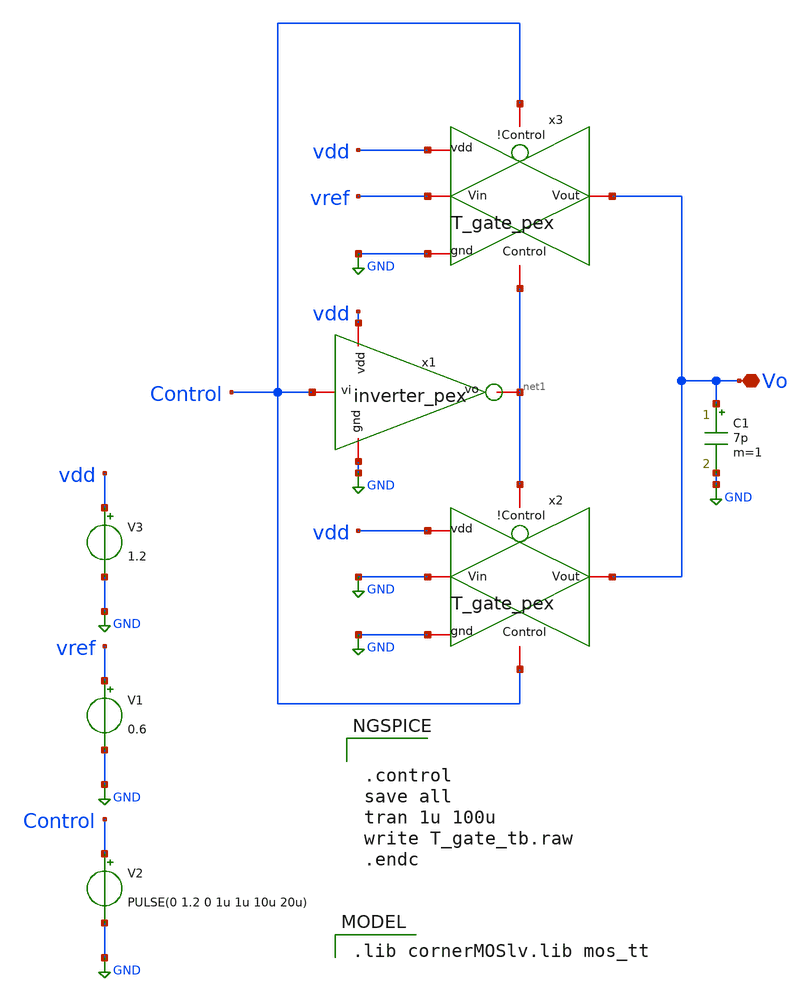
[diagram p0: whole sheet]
** sch_path: dependencies/ADC/ADC-main/schematic/xschem/T_gate_switch_tb_ps.sch
**.subckt T_gate_switch_tb_ps Vo
*.iopin Vo
V1 vref GND 0.6
V2 Control GND PULSE(0 1.2 0 1u 1u 10u 20u)
V3 vdd GND 1.2
C1 Vo GND 7p m=1
x1 vdd Control net1 GND inverter_pex
x2 net1 GND Vo GND Control vdd T_gate_pex
x3 Control vref Vo GND net1 vdd T_gate_pex
**** begin user architecture code


.control
save all
tran 1u 100u
write T_gate_tb.raw
.endc


 .lib cornerMOSlv.lib mos_tt

**** end user architecture code
**.ends

* expanding   symbol:  /home/tien/SAR_ADC_8BIT_IHP/xschem/xschem_pex_symbol/inverter_pex.sym # of
*+ pins=4
** sym_path: dependencies/ADC/dependencies/SAR_ADC_8BIT_IHP/pex/xschem_pex_symbol/inverter.sym

.subckt inverter_pex vdd vi vo gnd
X0 vo vi vdd vdd sg13_lv_pmos ad=0.272p pd=2.28u as=0.272p ps=2.28u w=0.8u l=0.13u
X1 vo vi gnd gnd sg13_lv_nmos ad=0.136p pd=1.48u as=0.136p ps=1.48u w=0.4u l=0.13u
C0 vo vdd 0.12375f
C1 vo vi 0.06195f
C2 vi vdd 0.09004f
C3 vo gnd 0.20432f
C4 vi gnd 0.35463f
C5 vdd gnd 0.1104f
.ends


* expanding   symbol:  /home/tien/SAR_ADC_8BIT_IHP/xschem/xschem_pex_symbol/T_gate_pex.sym # of
*+ pins=6
** sym_path: dependencies/ADC/ADC-main/schematic/xschem/xschem_pex_symbol/T_gate.sym

.subckt T_gate_pex Vin Vout Control gnd vdd
X0 Vout Control Vin gnd sg13_lv_nmos ad=0.34p pd=2.68u as=0.34p ps=2.68u w=1u l=0.13u
X1 Vout Control Vin vdd sg13_lv_pmos ad=0.68p pd=4.68u as=0.68p ps=4.68u w=2u l=0.13u
C0 Control vdd 0.06532f
C1 Vin Vout 0.44023f
C2 vdd Vout 0.19552f
C3 Control gnd 0.26277f
C4 Vout gnd 0.30897f
C5 Vin gnd 0.22881f
C6 Control gnd 0.30202f
C7 vdd gnd 0.09029f
.ends

.GLOBAL GND
.end
